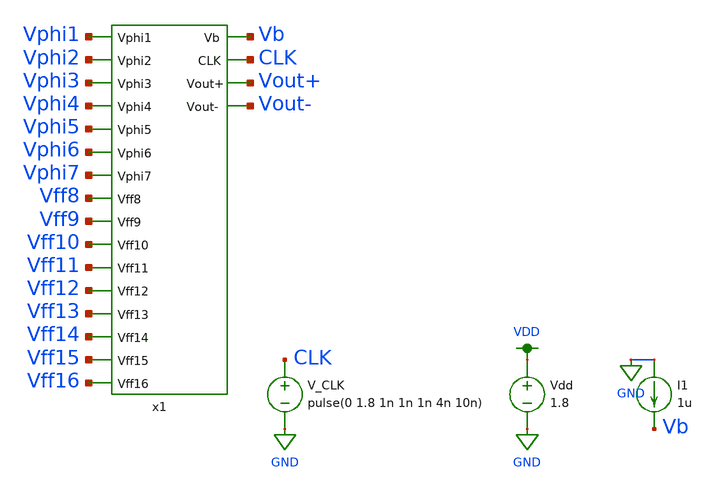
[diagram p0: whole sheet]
** sch_path: simulation/post_layout_sim/post_layout_mc.sch
**.subckt post_layout_mc
V_CLK CLK GND pulse(0 1.8 1n 1n 1n 4n 10n)
Vdd VDD GND 1.8
I1 GND Vb 1u
x1 Vphi1 Vphi2 Vphi3 Vphi4 Vphi5 Vphi6 Vphi7 Vff8 Vff9 Vff10 Vff11 Vff12 Vff13 Vff14 Vff15 Vff16 Vb
+ CLK Vout+ Vout- final
**** begin user architecture code

.option wnflag=1
.param MC_SWITCH=0.0
.lib ~/skywater/skywater-pdk/libraries/sky130_fd_pr_ngspice/latest/models/sky130.lib.spice tt



.ic v(Vphi1)=0 v(Vphi2)=0 v(Vphi3)=0 v(Vphi4)=0 v(Vphi5)=0 v(Vphi6)=0 v(Vphi7)=0 v(Vff8)=0
+ v(Vff9)=1.8 v(Vff10)=1.8 v(Vff11)=1.8 v(Vff12)=1.8 v(Vff13)=1.8 v(Vff14)=1.8 v(Vff15)=1.8 v(Vff16)=1.8
.control
  set wr_vecnames
  set wr_singlescale

  let mc_runs = 10
  let run = 1
  dowhile run <= mc_runs
    tran 0.1n 1u
    wrdata ~/VLSI_Sine_Gen/simulation/sim_data/mc_data/register_dac_mc_m0{$&run}.txt v(Vout+) v(Vout-)
+ v(Vout+)-v(Vout-)
    reset
    let run = run + 1
  end
  quit
.endc


**** end user architecture code
**.ends
.GLOBAL GND
.GLOBAL VDD
.end
